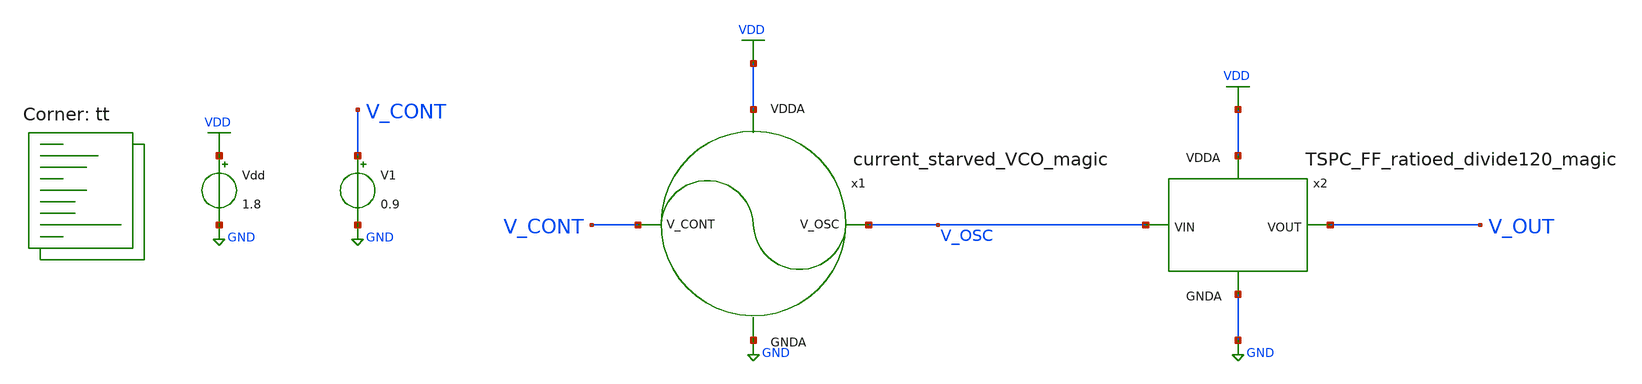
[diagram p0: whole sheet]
** sch_path: projects/pll/vco/magic/tb_current_starved_VCO_magic.sch
**.subckt tb_current_starved_VCO_magic
Vdd VDD GND 1.8
V1 V_CONT GND 0.9
x1 VDD V_OSC V_CONT GND current_starved_VCO_magic
x2 V_OUT V_OSC VDD GND TSPC_FF_ratioed_divide120_magic
**** begin user architecture code
.lib $::SKYWATER_MODELS/sky130.lib.spice tt



.include /foss/designs/my_design/projects/pll/vco/magic/current_starved_VCO_magic.spice
.include /foss/designs/my_design/projects/pll/divider/magic/divide_by_120/TSPC_FF_ratioed_divide120_magic.spice

.option method=trap
.option wnflag=1

.control

  let v_cont_start = 0.0
  let v_cont_stop = 1.9

  dowhile v_cont_start <= v_cont_stop
    alter v1 $&v_cont_start
    * save v(v_osc) v(v_cont) v(v_out)
    save all
    tran 5ps 30ns
    remzerovec
    write tb_current_starved_VCO_magic_{$&v_cont_start}.raw
    * write tb_current_starved_VCO_magic.raw
    linearize v(v_osc)
    let filename = v_cont_start * 100
    wrdata /foss/designs/my_design/projects/pll/vco/magic/tb_current_starved_VCO_magic_{$&filename}.txt
+ v(v_osc)
    * wrdata /foss/designs/my_design/projects/pll/vco/magic/tb_current_starved_VCO_magic.txt
+ v(v_osc)
    set appendwrite

    reset
    let v_cont_start = v_cont_start + 0.1
   end
.endc



**** end user architecture code
**.ends
.GLOBAL GND
.GLOBAL VDD
.end
